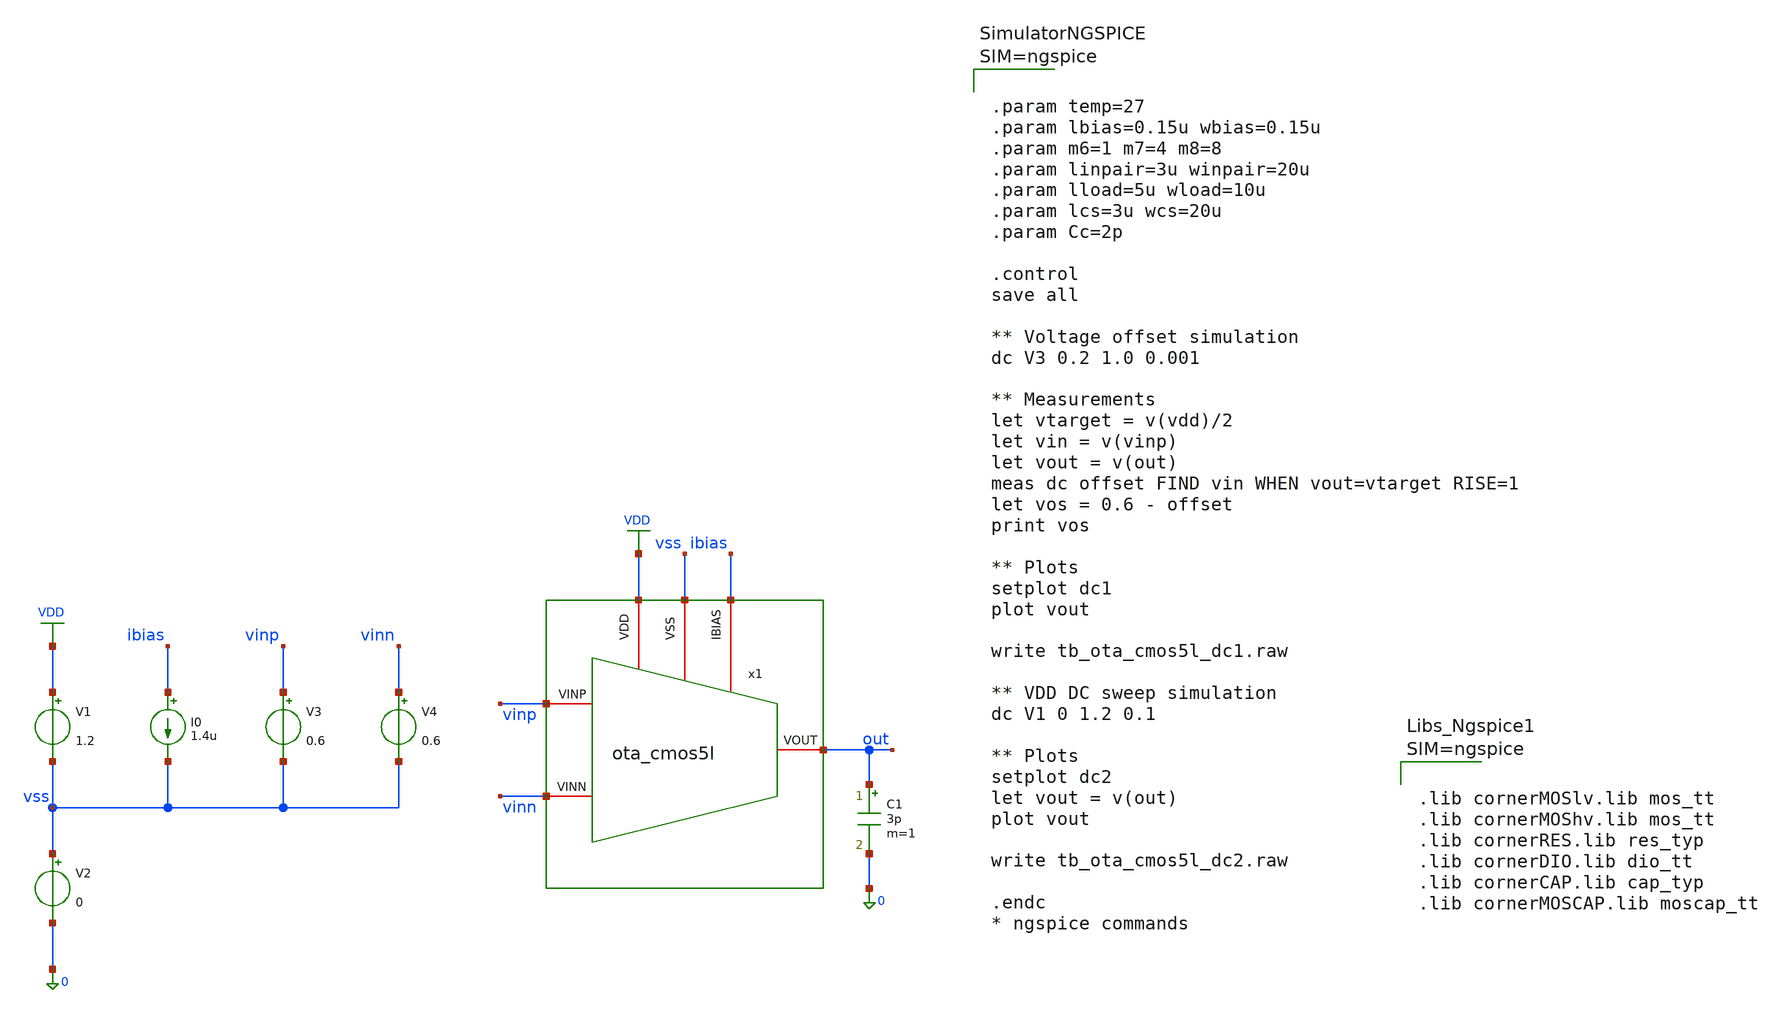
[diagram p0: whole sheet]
** sch_path: xschem/ota_cmos5l/tb/tb_ota_cmos5l_dc/tb_ota_cmos5l_dc.sch
**.subckt tb_ota_cmos5l_dc
x1 vss ibias VDD vinn vinp out ota_cmos5l
C1 out 0 3p m=1
I0 ibias vss 1.4u
V1 VDD vss 1.2
V2 vss 0 0
V3 vinp vss 0.6
V4 vinn vss 0.6
**** begin user architecture code



.param temp=27
.param lbias=0.15u wbias=0.15u
.param m6=1 m7=4 m8=8
.param linpair=3u winpair=20u
.param lload=5u wload=10u
.param lcs=3u wcs=20u
.param Cc=2p

.control
save all

** Voltage offset simulation
dc V3 0.2 1.0 0.001

** Measurements
let vtarget = v(vdd)/2
let vin = v(vinp)
let vout = v(out)
meas dc offset FIND vin WHEN vout=vtarget RISE=1
let vos = 0.6 - offset
print vos

** Plots
setplot dc1
plot vout

write tb_ota_cmos5l_dc1.raw

** VDD DC sweep simulation
dc V1 0 1.2 0.1

** Plots
setplot dc2
let vout = v(out)
plot vout

write tb_ota_cmos5l_dc2.raw

.endc
* ngspice commands






.lib cornerMOSlv.lib mos_tt
.lib cornerMOShv.lib mos_tt
.lib cornerRES.lib res_typ
.lib cornerDIO.lib dio_tt
.lib cornerCAP.lib cap_typ
.lib cornerMOSCAP.lib moscap_tt



**** end user architecture code
**.ends

* expanding   symbol:  /foss/designs/sg13cmos5l_spma_ip__instramp/xschem/ota_cmos5l/ota_cmos5l.sym #
*+ of pins=6
** sym_path: xschem/output_buffer/ota_cmos5l.sym
** sch_path: xschem/output_buffer/ota_cmos5l.sch
.subckt ota_cmos5l VSS IBIAS VDD VINN VINP VOUT
*.iopin IBIAS
*.iopin VDD
*.iopin VSS
*.iopin VOUT
*.iopin VINP
*.iopin VINN
XM6 IBIAS IBIAS VDD VDD sg13_lv_pmos w={wbias} l={lbias} ng=1 m={m6} mm_ok=1
XM7 net1 IBIAS VDD VDD sg13_lv_pmos w={wbias} l={lbias} ng=1 m={m7} mm_ok=1
XM8 VOUT IBIAS VDD VDD sg13_lv_pmos w={wbias} l={lbias} ng=1 m={m8} mm_ok=1
XM1 net2 VINN net1 VDD sg13_lv_pmos w={winpair} l={linpair} ng=1 m=1 mm_ok=1
XM2 net3 VINP net1 VDD sg13_lv_pmos w={winpair} l={linpair} ng=1 m=1 mm_ok=1
XM3 net2 net2 VSS VSS sg13_lv_nmos w={wload} l={lload} ng=1 m=1 mm_ok=1
XM4 net3 net2 VSS VSS sg13_lv_nmos w={wload} l={lload} ng=1 m=1 mm_ok=1
XM5 VOUT net3 VSS VSS sg13_lv_nmos w={wcs} l={lcs} ng=1 m=1 mm_ok=1
XR1 net3 net4 VSS rhigh w=0.5e-6 l=1.95e-6 m=1 b=0 mm_ok=1
.save v(vinp)
.save v(vinn)
.save v(vout)
XC2 VOUT net4 cap_cmomi w=15e-6 l=15e-6 mmin=1 mmax=4 feed=double subblock=0 m=5 mm_ok=1
**** begin user architecture code


.param temp=27
.param lbias=0.15u wbias=0.15u
.param m6=1 m7=4 m8=8
.param linpair=3u winpair=20u
.param lload=5u wload=10u
.param lcs=3u wcs=20u
.param Cc=2p



**** end user architecture code
XC1 VOUT net4 cap_cmomi w=15e-6 l=15e-6 mmin=1 mmax=4 feed=double subblock=0 m=4 mm_ok=1
.ends

.GLOBAL VDD
.end
